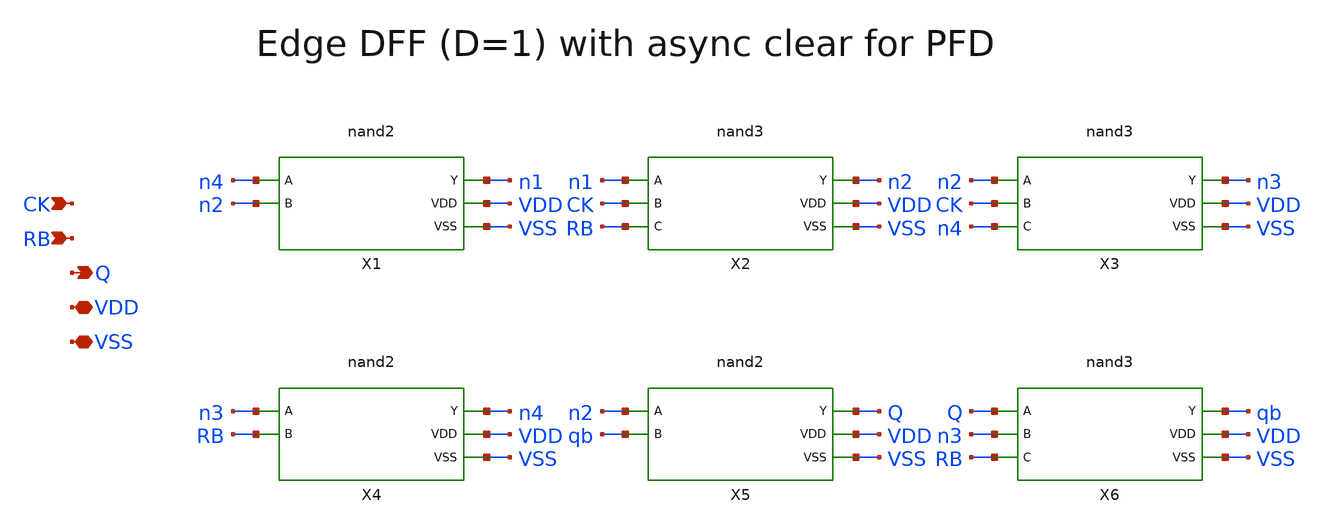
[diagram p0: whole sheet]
** sch_path: v1_claude/xschem/dff_r.sch
**.subckt dff_r CK RB Q VDD VSS
*.ipin CK
*.ipin RB
*.opin Q
*.iopin VDD
*.iopin VSS
X1 n4 n2 n1 VDD VSS nand2
X2 n1 CK RB n2 VDD VSS nand3
X3 n2 CK n4 n3 VDD VSS nand3
X4 n3 RB n4 VDD VSS nand2
X5 n2 qb Q VDD VSS nand2
X6 Q n3 RB qb VDD VSS nand3
**.ends

* expanding   symbol:  nand2.sym # of pins=5
** sym_path: v1_claude/xschem/nand2.sym
** sch_path: v1_claude/xschem/nand2.sch
.subckt nand2 A B Y VDD VSS
*.ipin A
*.ipin B
*.opin Y
*.iopin VDD
*.iopin VSS
XMN1 Y A n1 VSS nfet_03v3 L=0.28u W=2u nf=1 ad='int((nf+1)/2) * W/nf * 0.18u' as='int((nf+2)/2) * W/nf * 0.18u'
+ pd='2*int((nf+1)/2) * (W/nf + 0.18u)' ps='2*int((nf+2)/2) * (W/nf + 0.18u)' nrd='0.18u / W' nrs='0.18u / W'
+ sa=0 sb=0 sd=0 m=1
XMN2 n1 B VSS VSS nfet_03v3 L=0.28u W=2u nf=1 ad='int((nf+1)/2) * W/nf * 0.18u' as='int((nf+2)/2) * W/nf * 0.18u'
+ pd='2*int((nf+1)/2) * (W/nf + 0.18u)' ps='2*int((nf+2)/2) * (W/nf + 0.18u)' nrd='0.18u / W' nrs='0.18u / W'
+ sa=0 sb=0 sd=0 m=1
XMP1 Y A VDD VDD pfet_03v3 L=0.28u W=2u nf=1 ad='int((nf+1)/2) * W/nf * 0.18u' as='int((nf+2)/2) * W/nf * 0.18u'
+ pd='2*int((nf+1)/2) * (W/nf + 0.18u)' ps='2*int((nf+2)/2) * (W/nf + 0.18u)' nrd='0.18u / W' nrs='0.18u / W'
+ sa=0 sb=0 sd=0 m=1
XMP2 Y B VDD VDD pfet_03v3 L=0.28u W=2u nf=1 ad='int((nf+1)/2) * W/nf * 0.18u' as='int((nf+2)/2) * W/nf * 0.18u'
+ pd='2*int((nf+1)/2) * (W/nf + 0.18u)' ps='2*int((nf+2)/2) * (W/nf + 0.18u)' nrd='0.18u / W' nrs='0.18u / W'
+ sa=0 sb=0 sd=0 m=1
.ends


* expanding   symbol:  nand3.sym # of pins=6
** sym_path: v1_claude/xschem/nand3.sym
** sch_path: v1_claude/xschem/nand3.sch
.subckt nand3 A B C Y VDD VSS
*.ipin A
*.ipin B
*.ipin C
*.opin Y
*.iopin VDD
*.iopin VSS
XMN1 Y A n1 VSS nfet_03v3 L=0.28u W=3u nf=1 ad='int((nf+1)/2) * W/nf * 0.18u' as='int((nf+2)/2) * W/nf * 0.18u'
+ pd='2*int((nf+1)/2) * (W/nf + 0.18u)' ps='2*int((nf+2)/2) * (W/nf + 0.18u)' nrd='0.18u / W' nrs='0.18u / W'
+ sa=0 sb=0 sd=0 m=1
XMN2 n1 B n2 VSS nfet_03v3 L=0.28u W=3u nf=1 ad='int((nf+1)/2) * W/nf * 0.18u' as='int((nf+2)/2) * W/nf * 0.18u'
+ pd='2*int((nf+1)/2) * (W/nf + 0.18u)' ps='2*int((nf+2)/2) * (W/nf + 0.18u)' nrd='0.18u / W' nrs='0.18u / W'
+ sa=0 sb=0 sd=0 m=1
XMN3 n2 C VSS VSS nfet_03v3 L=0.28u W=3u nf=1 ad='int((nf+1)/2) * W/nf * 0.18u' as='int((nf+2)/2) * W/nf * 0.18u'
+ pd='2*int((nf+1)/2) * (W/nf + 0.18u)' ps='2*int((nf+2)/2) * (W/nf + 0.18u)' nrd='0.18u / W' nrs='0.18u / W'
+ sa=0 sb=0 sd=0 m=1
XMP1 Y A VDD VDD pfet_03v3 L=0.28u W=2u nf=1 ad='int((nf+1)/2) * W/nf * 0.18u' as='int((nf+2)/2) * W/nf * 0.18u'
+ pd='2*int((nf+1)/2) * (W/nf + 0.18u)' ps='2*int((nf+2)/2) * (W/nf + 0.18u)' nrd='0.18u / W' nrs='0.18u / W'
+ sa=0 sb=0 sd=0 m=1
XMP2 Y B VDD VDD pfet_03v3 L=0.28u W=2u nf=1 ad='int((nf+1)/2) * W/nf * 0.18u' as='int((nf+2)/2) * W/nf * 0.18u'
+ pd='2*int((nf+1)/2) * (W/nf + 0.18u)' ps='2*int((nf+2)/2) * (W/nf + 0.18u)' nrd='0.18u / W' nrs='0.18u / W'
+ sa=0 sb=0 sd=0 m=1
XMP3 Y C VDD VDD pfet_03v3 L=0.28u W=2u nf=1 ad='int((nf+1)/2) * W/nf * 0.18u' as='int((nf+2)/2) * W/nf * 0.18u'
+ pd='2*int((nf+1)/2) * (W/nf + 0.18u)' ps='2*int((nf+2)/2) * (W/nf + 0.18u)' nrd='0.18u / W' nrs='0.18u / W'
+ sa=0 sb=0 sd=0 m=1
.ends

.end
